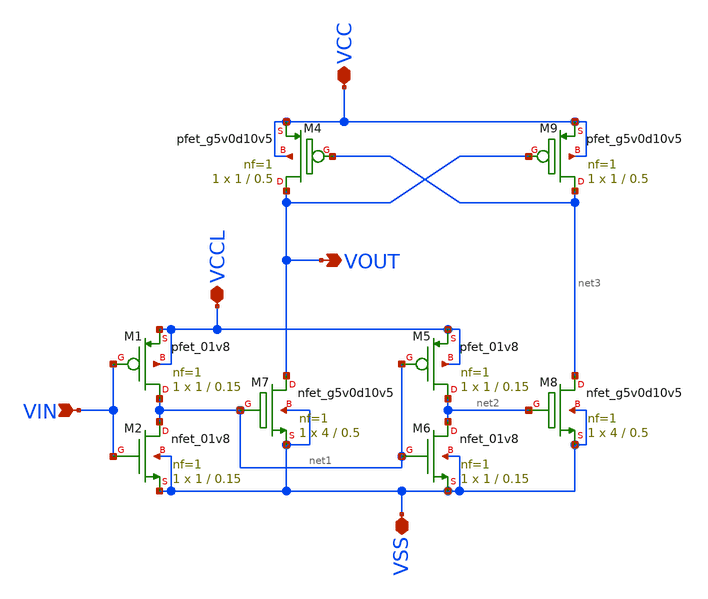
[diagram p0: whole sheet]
** sch_path: Layout_v2/lvs/All_schematic/level_translator.sch
**.subckt level_translator VCC VIN VOUT VCCL VSS
*.iopin VCC
*.ipin VIN
*.opin VOUT
*.iopin VCCL
*.iopin VSS
XM1 net1 VIN VCCL VCCL sky130_fd_pr__pfet_01v8 L=0.15 W=1 nf=1 ad='int((nf+1)/2) * W/nf * 0.29' as='int((nf+2)/2) * W/nf * 0.29'
+ pd='2*int((nf+1)/2) * (W/nf + 0.29)' ps='2*int((nf+2)/2) * (W/nf + 0.29)' nrd='0.29 / W' nrs='0.29 / W'
+ sa=0 sb=0 sd=0 mult=1 m=1
XM2 net1 VIN VSS VSS sky130_fd_pr__nfet_01v8 L=0.15 W=1 nf=1 ad='int((nf+1)/2) * W/nf * 0.29' as='int((nf+2)/2) * W/nf * 0.29'
+ pd='2*int((nf+1)/2) * (W/nf + 0.29)' ps='2*int((nf+2)/2) * (W/nf + 0.29)' nrd='0.29 / W' nrs='0.29 / W'
+ sa=0 sb=0 sd=0 mult=1 m=1
XM4 VOUT net3 VCC VCC sky130_fd_pr__pfet_g5v0d10v5 L=0.5 W=1 nf=1 ad='int((nf+1)/2) * W/nf * 0.29' as='int((nf+2)/2) * W/nf * 0.29'
+ pd='2*int((nf+1)/2) * (W/nf + 0.29)' ps='2*int((nf+2)/2) * (W/nf + 0.29)' nrd='0.29 / W' nrs='0.29 / W'
+ sa=0 sb=0 sd=0 mult=1 m=1
XM5 net2 net1 VCCL VCCL sky130_fd_pr__pfet_01v8 L=0.15 W=1 nf=1 ad='int((nf+1)/2) * W/nf * 0.29' as='int((nf+2)/2) * W/nf * 0.29'
+ pd='2*int((nf+1)/2) * (W/nf + 0.29)' ps='2*int((nf+2)/2) * (W/nf + 0.29)' nrd='0.29 / W' nrs='0.29 / W'
+ sa=0 sb=0 sd=0 mult=1 m=1
XM6 net2 net1 VSS VSS sky130_fd_pr__nfet_01v8 L=0.15 W=1 nf=1 ad='int((nf+1)/2) * W/nf * 0.29' as='int((nf+2)/2) * W/nf * 0.29'
+ pd='2*int((nf+1)/2) * (W/nf + 0.29)' ps='2*int((nf+2)/2) * (W/nf + 0.29)' nrd='0.29 / W' nrs='0.29 / W'
+ sa=0 sb=0 sd=0 mult=1 m=1
XM7 VOUT net1 VSS VSS sky130_fd_pr__nfet_g5v0d10v5 L=0.5 W=4 nf=1 ad='int((nf+1)/2) * W/nf * 0.29' as='int((nf+2)/2) * W/nf * 0.29'
+ pd='2*int((nf+1)/2) * (W/nf + 0.29)' ps='2*int((nf+2)/2) * (W/nf + 0.29)' nrd='0.29 / W' nrs='0.29 / W'
+ sa=0 sb=0 sd=0 mult=1 m=1
XM8 net3 net2 VSS VSS sky130_fd_pr__nfet_g5v0d10v5 L=0.5 W=4 nf=1 ad='int((nf+1)/2) * W/nf * 0.29' as='int((nf+2)/2) * W/nf * 0.29'
+ pd='2*int((nf+1)/2) * (W/nf + 0.29)' ps='2*int((nf+2)/2) * (W/nf + 0.29)' nrd='0.29 / W' nrs='0.29 / W'
+ sa=0 sb=0 sd=0 mult=1 m=1
XM9 net3 VOUT VCC VCC sky130_fd_pr__pfet_g5v0d10v5 L=0.5 W=1 nf=1 ad='int((nf+1)/2) * W/nf * 0.29' as='int((nf+2)/2) * W/nf * 0.29'
+ pd='2*int((nf+1)/2) * (W/nf + 0.29)' ps='2*int((nf+2)/2) * (W/nf + 0.29)' nrd='0.29 / W' nrs='0.29 / W'
+ sa=0 sb=0 sd=0 mult=1 m=1
**.ends
.end
